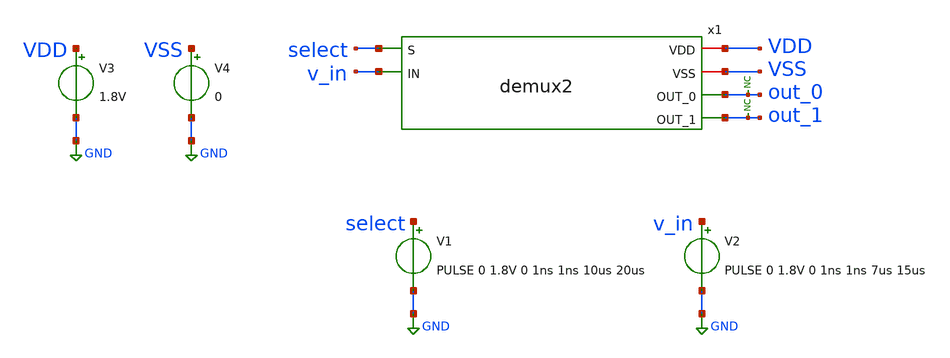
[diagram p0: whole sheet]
** sch_path: xschem/tests/demux2/demux2_xyce_test.sch
**.subckt demux2_xyce_test
V3 VDD GND 1.8V
V4 VSS GND 0
x1 select VDD VSS out_0 v_in out_1 demux2
V1 select GND PULSE 0 1.8V 0 1ns 1ns 10us 20us
V2 v_in GND PULSE 0 1.8V 0 1ns 1ns 7us 15us
* noconn out_0
* noconn out_1
**** begin user architecture code
 .lib $::SKYWATER_MODELS/sky130.lib.spice tt
.include $::SKYWATER_STDCELLS/sky130_fd_sc_hd.spice


.print TRAN FORMAT=RAW FILE=demux2_xyce_test.raw V(select) V(v_in) V(out_0) V(out_1)
.tran 1n 20u



**** end user architecture code
**.ends

* expanding   symbol:  src/demux2/demux2.sym # of pins=6
** sym_path: xschem/src/demux2/demux2.sym
** sch_path: xschem/src/demux2/demux2.sch
.subckt demux2 S VDD VSS OUT_0 IN OUT_1
*.ipin S
*.opin OUT_0
*.ipin IN
*.opin OUT_1
*.iopin VDD
*.iopin VSS
x1 net1 IN VSS VSS VDD VDD OUT_0 sky130_fd_sc_hd__and2_0
x2 S IN VSS VSS VDD VDD OUT_1 sky130_fd_sc_hd__and2_0
x3 S VSS VSS VDD VDD net1 sky130_fd_sc_hd__inv_1
.ends

.GLOBAL GND
.end
